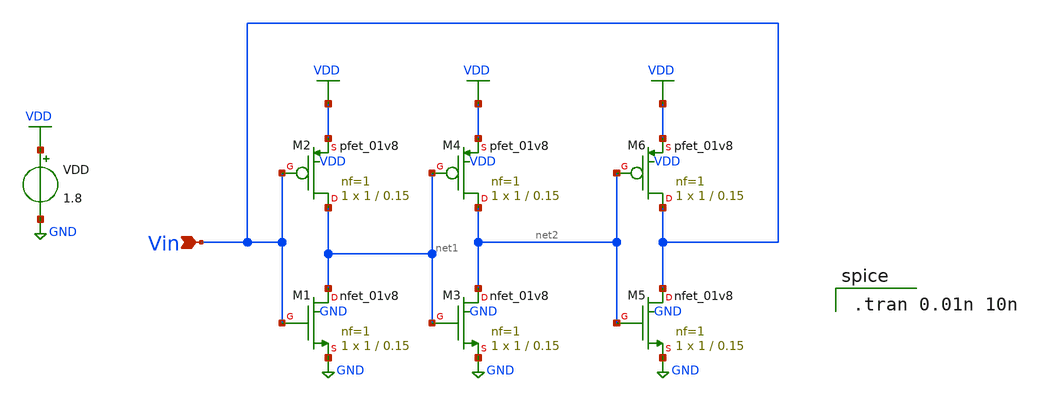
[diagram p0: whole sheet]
** sch_path: xschem/inverter_tutorial_trans.sch
**.subckt inverter_tutorial_trans Vin
*.ipin Vin
XM1 net1 Vin GND GND sky130_fd_pr__nfet_01v8 L=0.15 W=1 nf=1 ad='int((nf+1)/2) * W/nf * 0.29' as='int((nf+2)/2) * W/nf * 0.29'
+ pd='2*int((nf+1)/2) * (W/nf + 0.29)' ps='2*int((nf+2)/2) * (W/nf + 0.29)' nrd='0.29 / W' nrs='0.29 / W'
+ sa=0 sb=0 sd=0 mult=1 m=1
XM2 net1 Vin VDD VDD sky130_fd_pr__pfet_01v8 L=0.15 W=1 nf=1 ad='int((nf+1)/2) * W/nf * 0.29' as='int((nf+2)/2) * W/nf * 0.29'
+ pd='2*int((nf+1)/2) * (W/nf + 0.29)' ps='2*int((nf+2)/2) * (W/nf + 0.29)' nrd='0.29 / W' nrs='0.29 / W'
+ sa=0 sb=0 sd=0 mult=1 m=1
VDD VDD GND 1.8
XM3 net2 net1 GND GND sky130_fd_pr__nfet_01v8 L=0.15 W=1 nf=1 ad='int((nf+1)/2) * W/nf * 0.29' as='int((nf+2)/2) * W/nf * 0.29'
+ pd='2*int((nf+1)/2) * (W/nf + 0.29)' ps='2*int((nf+2)/2) * (W/nf + 0.29)' nrd='0.29 / W' nrs='0.29 / W'
+ sa=0 sb=0 sd=0 mult=1 m=1
XM4 net2 net1 VDD VDD sky130_fd_pr__pfet_01v8 L=0.15 W=1 nf=1 ad='int((nf+1)/2) * W/nf * 0.29' as='int((nf+2)/2) * W/nf * 0.29'
+ pd='2*int((nf+1)/2) * (W/nf + 0.29)' ps='2*int((nf+2)/2) * (W/nf + 0.29)' nrd='0.29 / W' nrs='0.29 / W'
+ sa=0 sb=0 sd=0 mult=1 m=1
XM5 Vin net2 GND GND sky130_fd_pr__nfet_01v8 L=0.15 W=1 nf=1 ad='int((nf+1)/2) * W/nf * 0.29' as='int((nf+2)/2) * W/nf * 0.29'
+ pd='2*int((nf+1)/2) * (W/nf + 0.29)' ps='2*int((nf+2)/2) * (W/nf + 0.29)' nrd='0.29 / W' nrs='0.29 / W'
+ sa=0 sb=0 sd=0 mult=1 m=1
XM6 Vin net2 VDD VDD sky130_fd_pr__pfet_01v8 L=0.15 W=1 nf=1 ad='int((nf+1)/2) * W/nf * 0.29' as='int((nf+2)/2) * W/nf * 0.29'
+ pd='2*int((nf+1)/2) * (W/nf + 0.29)' ps='2*int((nf+2)/2) * (W/nf + 0.29)' nrd='0.29 / W' nrs='0.29 / W'
+ sa=0 sb=0 sd=0 mult=1 m=1
**** begin user architecture code

** opencircuitdesign pdks install
.lib $::SKYWATER_MODELS/sky130.lib.spice tt



.tran 0.01n 10n

**** end user architecture code
**.ends
.GLOBAL GND
.GLOBAL VDD
.end
